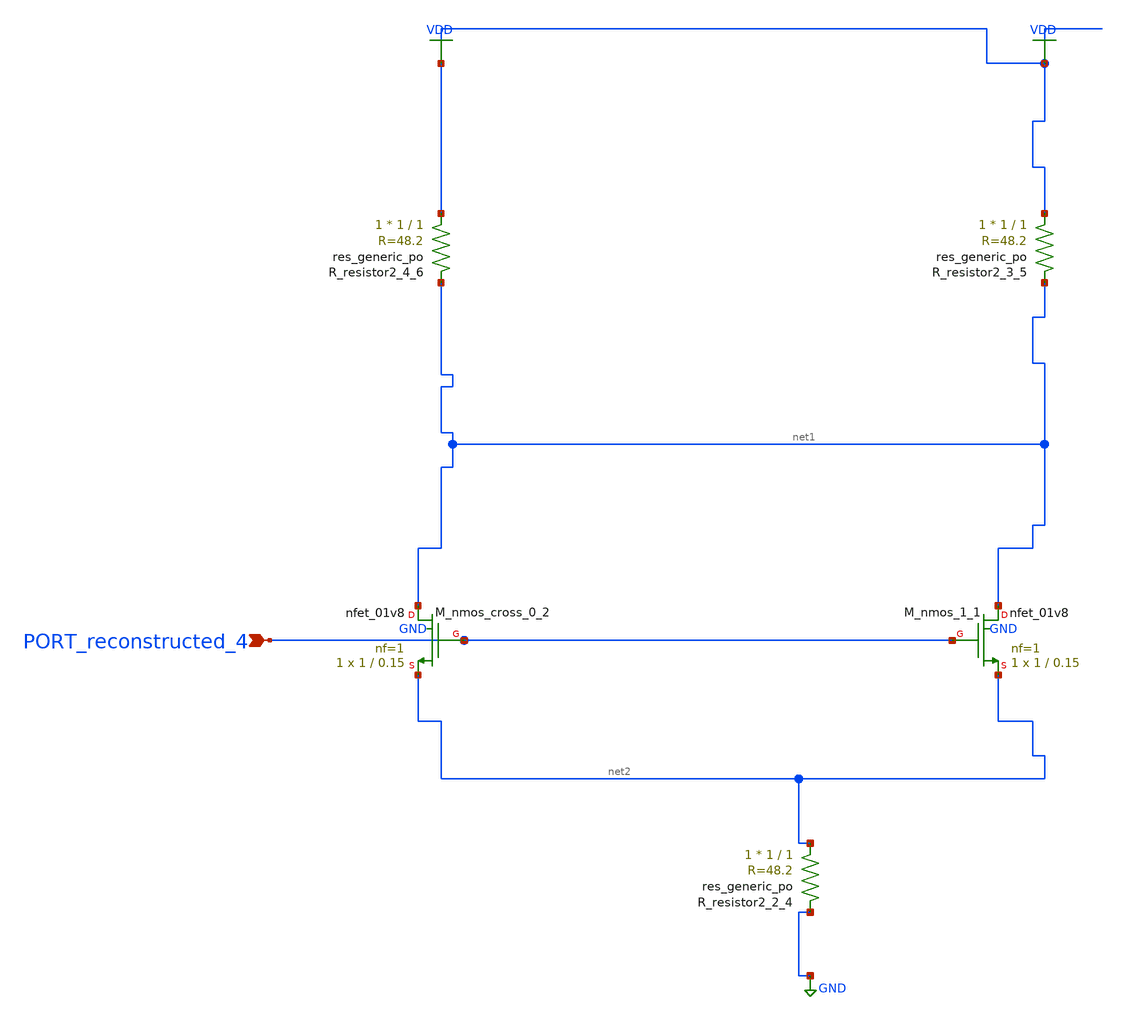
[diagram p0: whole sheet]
** sch_path: schematics/AMSNet/211.sch
**.subckt 211 PORT_reconstructed_4
*.ipin PORT_reconstructed_4
XM_nmos_1_1 net1 PORT_reconstructed_4 net2 GND sky130_fd_pr__nfet_01v8 L=0.15 W=1 nf=1 ad='int((1 + 1)/2) * 1 / 1 * 0.29'
+ as='int((1 + 2)/2) * 1 / 1 * 0.29' pd='2*int((1 + 1)/2) * (1 / 1 + 0.29)' ps='2*int((1 + 2)/2) * (1 / 1 + 0.29)'
+ nrd='0.29 / 1 ' nrs='0.29 / 1 ' sa=0 sb=0 sd=0 mult=1 m=1
XM_nmos_cross_0_2 net1 PORT_reconstructed_4 net2 GND sky130_fd_pr__nfet_01v8 L=0.15 W=1 nf=1 ad='int((1 + 1)/2) * 1 / 1 * 0.29'
+ as='int((1 + 2)/2) * 1 / 1 * 0.29' pd='2*int((1 + 1)/2) * (1 / 1 + 0.29)' ps='2*int((1 + 2)/2) * (1 / 1 + 0.29)'
+ nrd='0.29 / 1 ' nrs='0.29 / 1 ' sa=0 sb=0 sd=0 mult=1 m=1
XR_resistor2_2_4 net2 GND sky130_fd_pr__res_generic_po W=1 L=1 m=1
XR_resistor2_3_5 VDD net1 sky130_fd_pr__res_generic_po W=1 L=1 m=1
XR_resistor2_4_6 VDD net1 sky130_fd_pr__res_generic_po W=1 L=1 m=1
**.ends
.GLOBAL GND
.GLOBAL VDD
.end
